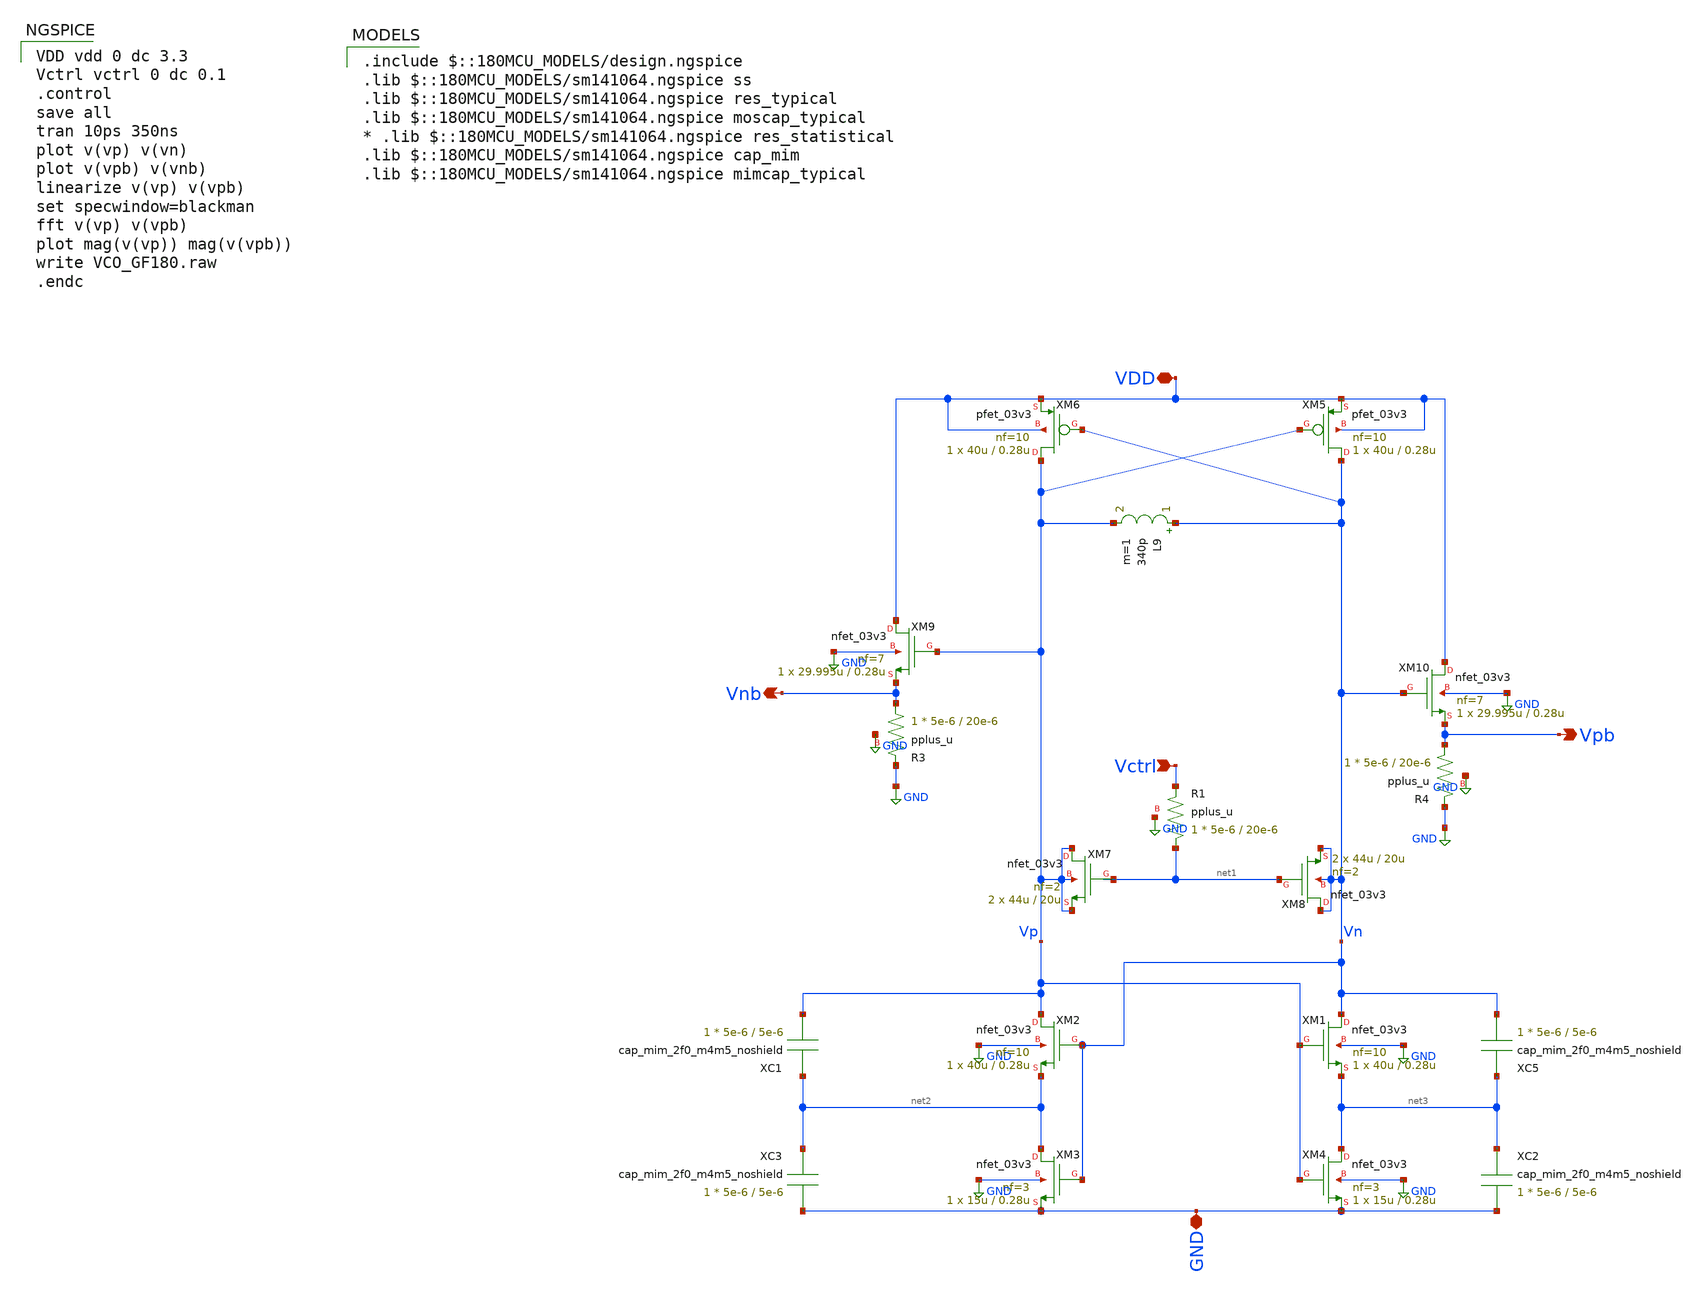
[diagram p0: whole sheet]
** sch_path: blocks/pll/vco.sch
**.subckt vco VDD GND Vctrl Vpb Vnb
*.iopin VDD
*.iopin GND
*.ipin Vctrl
*.opin Vpb
*.opin Vnb
XM1 Vn Vp net3 GND nfet_03v3 L=0.28u W=40u nf=10 ad='int((nf+1)/2) * W/nf * 0.18u' as='int((nf+2)/2) * W/nf * 0.18u'
+ pd='2*int((nf+1)/2) * (W/nf + 0.18u)' ps='2*int((nf+2)/2) * (W/nf + 0.18u)' nrd='0.18u / W' nrs='0.18u / W'
+ sa=0 sb=0 sd=0 m=1
XM2 Vp Vn net2 GND nfet_03v3 L=0.28u W=40u nf=10 ad='int((nf+1)/2) * W/nf * 0.18u' as='int((nf+2)/2) * W/nf * 0.18u'
+ pd='2*int((nf+1)/2) * (W/nf + 0.18u)' ps='2*int((nf+2)/2) * (W/nf + 0.18u)' nrd='0.18u / W' nrs='0.18u / W'
+ sa=0 sb=0 sd=0 m=1
XM3 net2 Vn GND GND nfet_03v3 L=0.28u W=15u nf=3 ad='int((nf+1)/2) * W/nf * 0.18u' as='int((nf+2)/2) * W/nf * 0.18u'
+ pd='2*int((nf+1)/2) * (W/nf + 0.18u)' ps='2*int((nf+2)/2) * (W/nf + 0.18u)' nrd='0.18u / W' nrs='0.18u / W'
+ sa=0 sb=0 sd=0 m=1
XM4 net3 Vp GND GND nfet_03v3 L=0.28u W=15u nf=3 ad='int((nf+1)/2) * W/nf * 0.18u' as='int((nf+2)/2) * W/nf * 0.18u'
+ pd='2*int((nf+1)/2) * (W/nf + 0.18u)' ps='2*int((nf+2)/2) * (W/nf + 0.18u)' nrd='0.18u / W' nrs='0.18u / W'
+ sa=0 sb=0 sd=0 m=1
XR1 net1 Vctrl GND pplus_u r_width=5e-6 r_length=20e-6 m=1
XM5 Vn Vp VDD VDD pfet_03v3 L=0.28u W=40u nf=10 ad='int((nf+1)/2) * W/nf * 0.18u' as='int((nf+2)/2) * W/nf * 0.18u'
+ pd='2*int((nf+1)/2) * (W/nf + 0.18u)' ps='2*int((nf+2)/2) * (W/nf + 0.18u)' nrd='0.18u / W' nrs='0.18u / W'
+ sa=0 sb=0 sd=0 m=1
XM6 Vp Vn VDD VDD pfet_03v3 L=0.28u W=40u nf=10 ad='int((nf+1)/2) * W/nf * 0.18u' as='int((nf+2)/2) * W/nf * 0.18u'
+ pd='2*int((nf+1)/2) * (W/nf + 0.18u)' ps='2*int((nf+2)/2) * (W/nf + 0.18u)' nrd='0.18u / W' nrs='0.18u / W'
+ sa=0 sb=0 sd=0 m=1
L9 Vn Vp 340p m=1
XM7 Vp net1 Vp Vp nfet_03v3 L=20u W=44u nf=2 ad='int((nf+1)/2) * W/nf * 0.18u' as='int((nf+2)/2) * W/nf * 0.18u'
+ pd='2*int((nf+1)/2) * (W/nf + 0.18u)' ps='2*int((nf+2)/2) * (W/nf + 0.18u)' nrd='0.18u / W' nrs='0.18u / W'
+ sa=0 sb=0 sd=0 m=2
XM8 Vn net1 Vn Vn nfet_03v3 L=20u W=44u nf=2 ad='int((nf+1)/2) * W/nf * 0.18u' as='int((nf+2)/2) * W/nf * 0.18u'
+ pd='2*int((nf+1)/2) * (W/nf + 0.18u)' ps='2*int((nf+2)/2) * (W/nf + 0.18u)' nrd='0.18u / W' nrs='0.18u / W'
+ sa=0 sb=0 sd=0 m=2
XM9 VDD Vp Vnb GND nfet_03v3 L=0.28u W=29.995u nf=7 ad='int((nf+1)/2) * W/nf * 0.18u' as='int((nf+2)/2) * W/nf * 0.18u'
+ pd='2*int((nf+1)/2) * (W/nf + 0.18u)' ps='2*int((nf+2)/2) * (W/nf + 0.18u)' nrd='0.18u / W' nrs='0.18u / W'
+ sa=0 sb=0 sd=0 m=1
XR3 Vnb GND GND pplus_u r_width=5e-6 r_length=20e-6 m=1
XM10 VDD Vn Vpb GND nfet_03v3 L=0.28u W=29.995u nf=7 ad='int((nf+1)/2) * W/nf * 0.18u' as='int((nf+2)/2) * W/nf * 0.18u'
+ pd='2*int((nf+1)/2) * (W/nf + 0.18u)' ps='2*int((nf+2)/2) * (W/nf + 0.18u)' nrd='0.18u / W' nrs='0.18u / W'
+ sa=0 sb=0 sd=0 m=1
XR4 Vpb GND GND pplus_u r_width=5e-6 r_length=20e-6 m=1
XC5 net3 Vn cap_mim_2f0_m4m5_noshield c_width=5e-6 c_length=5e-6 m=1
XC2 net3 GND cap_mim_2f0_m4m5_noshield c_width=5e-6 c_length=5e-6 m=1
XC3 net2 GND cap_mim_2f0_m4m5_noshield c_width=5e-6 c_length=5e-6 m=1
XC1 net2 Vp cap_mim_2f0_m4m5_noshield c_width=5e-6 c_length=5e-6 m=1
**** begin user architecture code
 .include $::180MCU_MODELS/design.ngspice
.lib $::180MCU_MODELS/sm141064.ngspice ss
.lib $::180MCU_MODELS/sm141064.ngspice res_typical
.lib $::180MCU_MODELS/sm141064.ngspice moscap_typical
* .lib $::180MCU_MODELS/sm141064.ngspice res_statistical
.lib $::180MCU_MODELS/sm141064.ngspice cap_mim
.lib $::180MCU_MODELS/sm141064.ngspice mimcap_typical


VDD vdd 0 dc 3.3
Vctrl vctrl 0 dc 0.1
.control
save all
tran 10ps 350ns
plot v(vp) v(vn)
plot v(vpb) v(vnb)
linearize v(vp) v(vpb)
set specwindow=blackman
fft v(vp) v(vpb)
plot mag(v(vp)) mag(v(vpb))
write VCO_GF180.raw
.endc


**** end user architecture code
**.ends
.GLOBAL GND
.end
